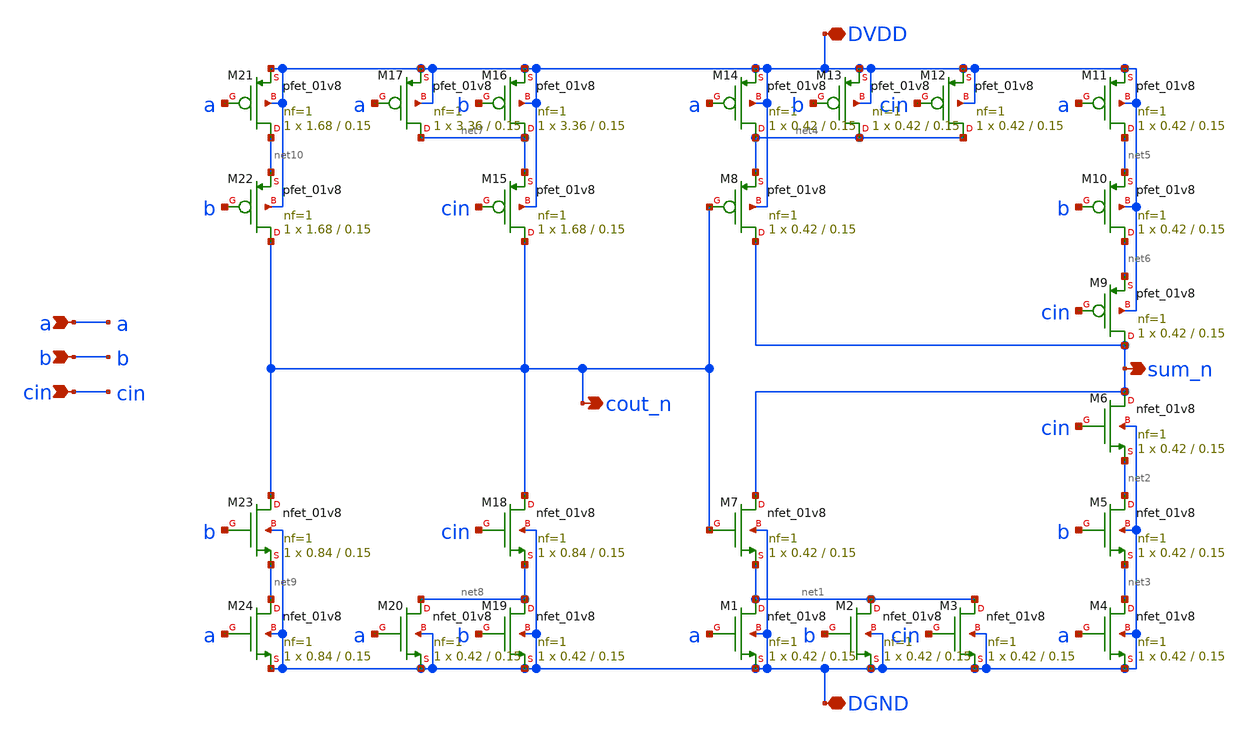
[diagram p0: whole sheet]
** sch_path: tut6/incr/step4/fa.sch
**.subckt fa a b cin DGND DVDD sum_n cout_n
*.ipin a
*.ipin b
*.ipin cin
*.iopin DGND
*.iopin DVDD
*.opin sum_n
*.opin cout_n
XM1 net1 a DGND DGND sky130_fd_pr__nfet_01v8 L=0.15 W=0.42 nf=1 ad='int((nf+1)/2) * W/nf * 0.29' as='int((nf+2)/2) * W/nf * 0.29'
+ pd='2*int((nf+1)/2) * (W/nf + 0.29)' ps='2*int((nf+2)/2) * (W/nf + 0.29)' nrd='0.29 / W' nrs='0.29 / W'
+ sa=0 sb=0 sd=0 mult=1 m=1
XM2 net1 b DGND DGND sky130_fd_pr__nfet_01v8 L=0.15 W=0.42 nf=1 ad='int((nf+1)/2) * W/nf * 0.29' as='int((nf+2)/2) * W/nf * 0.29'
+ pd='2*int((nf+1)/2) * (W/nf + 0.29)' ps='2*int((nf+2)/2) * (W/nf + 0.29)' nrd='0.29 / W' nrs='0.29 / W'
+ sa=0 sb=0 sd=0 mult=1 m=1
XM3 net1 cin DGND DGND sky130_fd_pr__nfet_01v8 L=0.15 W=0.42 nf=1 ad='int((nf+1)/2) * W/nf * 0.29' as='int((nf+2)/2) * W/nf * 0.29'
+ pd='2*int((nf+1)/2) * (W/nf + 0.29)' ps='2*int((nf+2)/2) * (W/nf + 0.29)' nrd='0.29 / W' nrs='0.29 / W'
+ sa=0 sb=0 sd=0 mult=1 m=1
XM4 net3 a DGND DGND sky130_fd_pr__nfet_01v8 L=0.15 W=0.42 nf=1 ad='int((nf+1)/2) * W/nf * 0.29' as='int((nf+2)/2) * W/nf * 0.29'
+ pd='2*int((nf+1)/2) * (W/nf + 0.29)' ps='2*int((nf+2)/2) * (W/nf + 0.29)' nrd='0.29 / W' nrs='0.29 / W'
+ sa=0 sb=0 sd=0 mult=1 m=1
XM5 net2 b net3 DGND sky130_fd_pr__nfet_01v8 L=0.15 W=0.42 nf=1 ad='int((nf+1)/2) * W/nf * 0.29' as='int((nf+2)/2) * W/nf * 0.29'
+ pd='2*int((nf+1)/2) * (W/nf + 0.29)' ps='2*int((nf+2)/2) * (W/nf + 0.29)' nrd='0.29 / W' nrs='0.29 / W'
+ sa=0 sb=0 sd=0 mult=1 m=1
XM6 sum_n cin net2 DGND sky130_fd_pr__nfet_01v8 L=0.15 W=0.42 nf=1 ad='int((nf+1)/2) * W/nf * 0.29' as='int((nf+2)/2) * W/nf * 0.29'
+ pd='2*int((nf+1)/2) * (W/nf + 0.29)' ps='2*int((nf+2)/2) * (W/nf + 0.29)' nrd='0.29 / W' nrs='0.29 / W'
+ sa=0 sb=0 sd=0 mult=1 m=1
XM7 sum_n cout_n net1 DGND sky130_fd_pr__nfet_01v8 L=0.15 W=0.42 nf=1 ad='int((nf+1)/2) * W/nf * 0.29'
+ as='int((nf+2)/2) * W/nf * 0.29' pd='2*int((nf+1)/2) * (W/nf + 0.29)' ps='2*int((nf+2)/2) * (W/nf + 0.29)'
+ nrd='0.29 / W' nrs='0.29 / W' sa=0 sb=0 sd=0 mult=1 m=1
XM8 sum_n cout_n net4 DVDD sky130_fd_pr__pfet_01v8 L=0.15 W=0.42 nf=1 ad='int((nf+1)/2) * W/nf * 0.29'
+ as='int((nf+2)/2) * W/nf * 0.29' pd='2*int((nf+1)/2) * (W/nf + 0.29)' ps='2*int((nf+2)/2) * (W/nf + 0.29)'
+ nrd='0.29 / W' nrs='0.29 / W' sa=0 sb=0 sd=0 mult=1 m=1
XM9 sum_n cin net6 DVDD sky130_fd_pr__pfet_01v8 L=0.15 W=0.42 nf=1 ad='int((nf+1)/2) * W/nf * 0.29' as='int((nf+2)/2) * W/nf * 0.29'
+ pd='2*int((nf+1)/2) * (W/nf + 0.29)' ps='2*int((nf+2)/2) * (W/nf + 0.29)' nrd='0.29 / W' nrs='0.29 / W'
+ sa=0 sb=0 sd=0 mult=1 m=1
XM10 net6 b net5 DVDD sky130_fd_pr__pfet_01v8 L=0.15 W=0.42 nf=1 ad='int((nf+1)/2) * W/nf * 0.29' as='int((nf+2)/2) * W/nf * 0.29'
+ pd='2*int((nf+1)/2) * (W/nf + 0.29)' ps='2*int((nf+2)/2) * (W/nf + 0.29)' nrd='0.29 / W' nrs='0.29 / W'
+ sa=0 sb=0 sd=0 mult=1 m=1
XM11 net5 a DVDD DVDD sky130_fd_pr__pfet_01v8 L=0.15 W=0.42 nf=1 ad='int((nf+1)/2) * W/nf * 0.29' as='int((nf+2)/2) * W/nf * 0.29'
+ pd='2*int((nf+1)/2) * (W/nf + 0.29)' ps='2*int((nf+2)/2) * (W/nf + 0.29)' nrd='0.29 / W' nrs='0.29 / W'
+ sa=0 sb=0 sd=0 mult=1 m=1
XM12 net4 cin DVDD DVDD sky130_fd_pr__pfet_01v8 L=0.15 W=0.42 nf=1 ad='int((nf+1)/2) * W/nf * 0.29' as='int((nf+2)/2) * W/nf * 0.29'
+ pd='2*int((nf+1)/2) * (W/nf + 0.29)' ps='2*int((nf+2)/2) * (W/nf + 0.29)' nrd='0.29 / W' nrs='0.29 / W'
+ sa=0 sb=0 sd=0 mult=1 m=1
XM13 net4 b DVDD DVDD sky130_fd_pr__pfet_01v8 L=0.15 W=0.42 nf=1 ad='int((nf+1)/2) * W/nf * 0.29' as='int((nf+2)/2) * W/nf * 0.29'
+ pd='2*int((nf+1)/2) * (W/nf + 0.29)' ps='2*int((nf+2)/2) * (W/nf + 0.29)' nrd='0.29 / W' nrs='0.29 / W'
+ sa=0 sb=0 sd=0 mult=1 m=1
XM14 net4 a DVDD DVDD sky130_fd_pr__pfet_01v8 L=0.15 W=0.42 nf=1 ad='int((nf+1)/2) * W/nf * 0.29' as='int((nf+2)/2) * W/nf * 0.29'
+ pd='2*int((nf+1)/2) * (W/nf + 0.29)' ps='2*int((nf+2)/2) * (W/nf + 0.29)' nrd='0.29 / W' nrs='0.29 / W'
+ sa=0 sb=0 sd=0 mult=1 m=1
XM15 cout_n cin net7 DVDD sky130_fd_pr__pfet_01v8 L=0.15 W=1.68 nf=1 ad='int((nf+1)/2) * W/nf * 0.29'
+ as='int((nf+2)/2) * W/nf * 0.29' pd='2*int((nf+1)/2) * (W/nf + 0.29)' ps='2*int((nf+2)/2) * (W/nf + 0.29)'
+ nrd='0.29 / W' nrs='0.29 / W' sa=0 sb=0 sd=0 mult=1 m=1
XM16 net7 b DVDD DVDD sky130_fd_pr__pfet_01v8 L=0.15 W=3.36 nf=1 ad='int((nf+1)/2) * W/nf * 0.29' as='int((nf+2)/2) * W/nf * 0.29'
+ pd='2*int((nf+1)/2) * (W/nf + 0.29)' ps='2*int((nf+2)/2) * (W/nf + 0.29)' nrd='0.29 / W' nrs='0.29 / W'
+ sa=0 sb=0 sd=0 mult=1 m=1
XM17 net7 a DVDD DVDD sky130_fd_pr__pfet_01v8 L=0.15 W=3.36 nf=1 ad='int((nf+1)/2) * W/nf * 0.29' as='int((nf+2)/2) * W/nf * 0.29'
+ pd='2*int((nf+1)/2) * (W/nf + 0.29)' ps='2*int((nf+2)/2) * (W/nf + 0.29)' nrd='0.29 / W' nrs='0.29 / W'
+ sa=0 sb=0 sd=0 mult=1 m=1
XM18 cout_n cin net8 DGND sky130_fd_pr__nfet_01v8 L=0.15 W=0.84 nf=1 ad='int((nf+1)/2) * W/nf * 0.29'
+ as='int((nf+2)/2) * W/nf * 0.29' pd='2*int((nf+1)/2) * (W/nf + 0.29)' ps='2*int((nf+2)/2) * (W/nf + 0.29)'
+ nrd='0.29 / W' nrs='0.29 / W' sa=0 sb=0 sd=0 mult=1 m=1
XM19 net8 b DGND DGND sky130_fd_pr__nfet_01v8 L=0.15 W=0.42 nf=1 ad='int((nf+1)/2) * W/nf * 0.29' as='int((nf+2)/2) * W/nf * 0.29'
+ pd='2*int((nf+1)/2) * (W/nf + 0.29)' ps='2*int((nf+2)/2) * (W/nf + 0.29)' nrd='0.29 / W' nrs='0.29 / W'
+ sa=0 sb=0 sd=0 mult=1 m=1
XM20 net8 a DGND DGND sky130_fd_pr__nfet_01v8 L=0.15 W=0.42 nf=1 ad='int((nf+1)/2) * W/nf * 0.29' as='int((nf+2)/2) * W/nf * 0.29'
+ pd='2*int((nf+1)/2) * (W/nf + 0.29)' ps='2*int((nf+2)/2) * (W/nf + 0.29)' nrd='0.29 / W' nrs='0.29 / W'
+ sa=0 sb=0 sd=0 mult=1 m=1
XM21 net10 a DVDD DVDD sky130_fd_pr__pfet_01v8 L=0.15 W=1.68 nf=1 ad='int((nf+1)/2) * W/nf * 0.29' as='int((nf+2)/2) * W/nf * 0.29'
+ pd='2*int((nf+1)/2) * (W/nf + 0.29)' ps='2*int((nf+2)/2) * (W/nf + 0.29)' nrd='0.29 / W' nrs='0.29 / W'
+ sa=0 sb=0 sd=0 mult=1 m=1
XM22 cout_n b net10 DVDD sky130_fd_pr__pfet_01v8 L=0.15 W=1.68 nf=1 ad='int((nf+1)/2) * W/nf * 0.29'
+ as='int((nf+2)/2) * W/nf * 0.29' pd='2*int((nf+1)/2) * (W/nf + 0.29)' ps='2*int((nf+2)/2) * (W/nf + 0.29)'
+ nrd='0.29 / W' nrs='0.29 / W' sa=0 sb=0 sd=0 mult=1 m=1
XM23 cout_n b net9 DGND sky130_fd_pr__nfet_01v8 L=0.15 W=0.84 nf=1 ad='int((nf+1)/2) * W/nf * 0.29' as='int((nf+2)/2) * W/nf * 0.29'
+ pd='2*int((nf+1)/2) * (W/nf + 0.29)' ps='2*int((nf+2)/2) * (W/nf + 0.29)' nrd='0.29 / W' nrs='0.29 / W'
+ sa=0 sb=0 sd=0 mult=1 m=1
XM24 net9 a DGND DGND sky130_fd_pr__nfet_01v8 L=0.15 W=0.84 nf=1 ad='int((nf+1)/2) * W/nf * 0.29' as='int((nf+2)/2) * W/nf * 0.29'
+ pd='2*int((nf+1)/2) * (W/nf + 0.29)' ps='2*int((nf+2)/2) * (W/nf + 0.29)' nrd='0.29 / W' nrs='0.29 / W'
+ sa=0 sb=0 sd=0 mult=1 m=1
**.ends
.end
